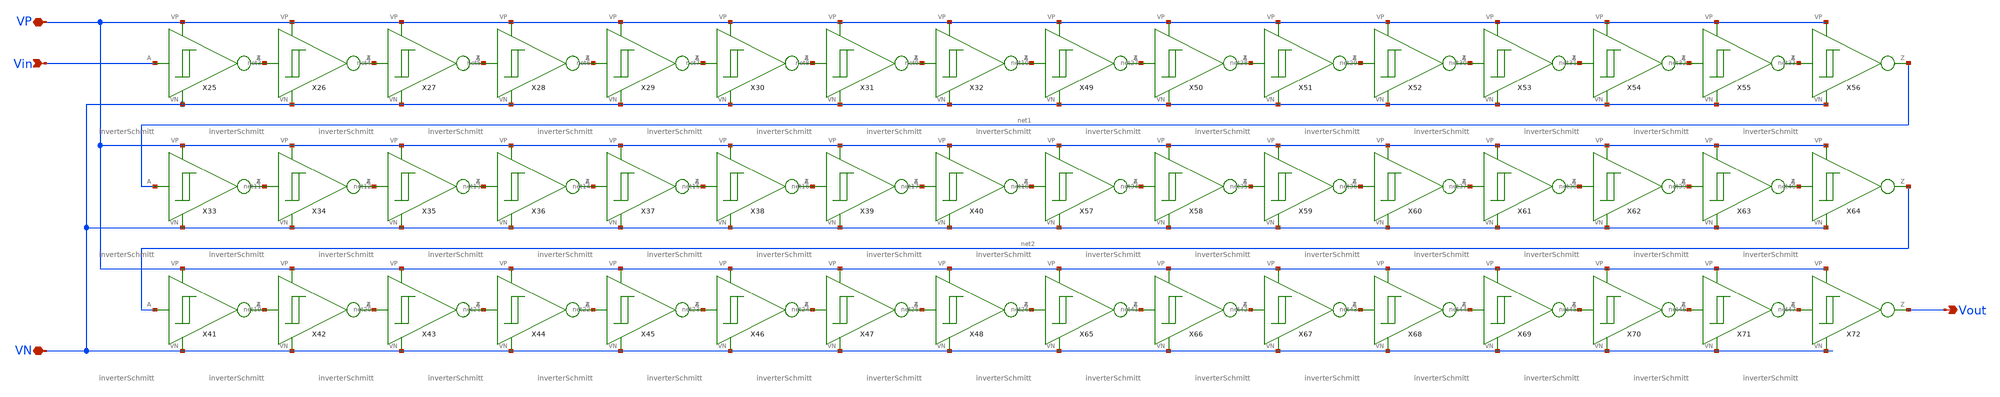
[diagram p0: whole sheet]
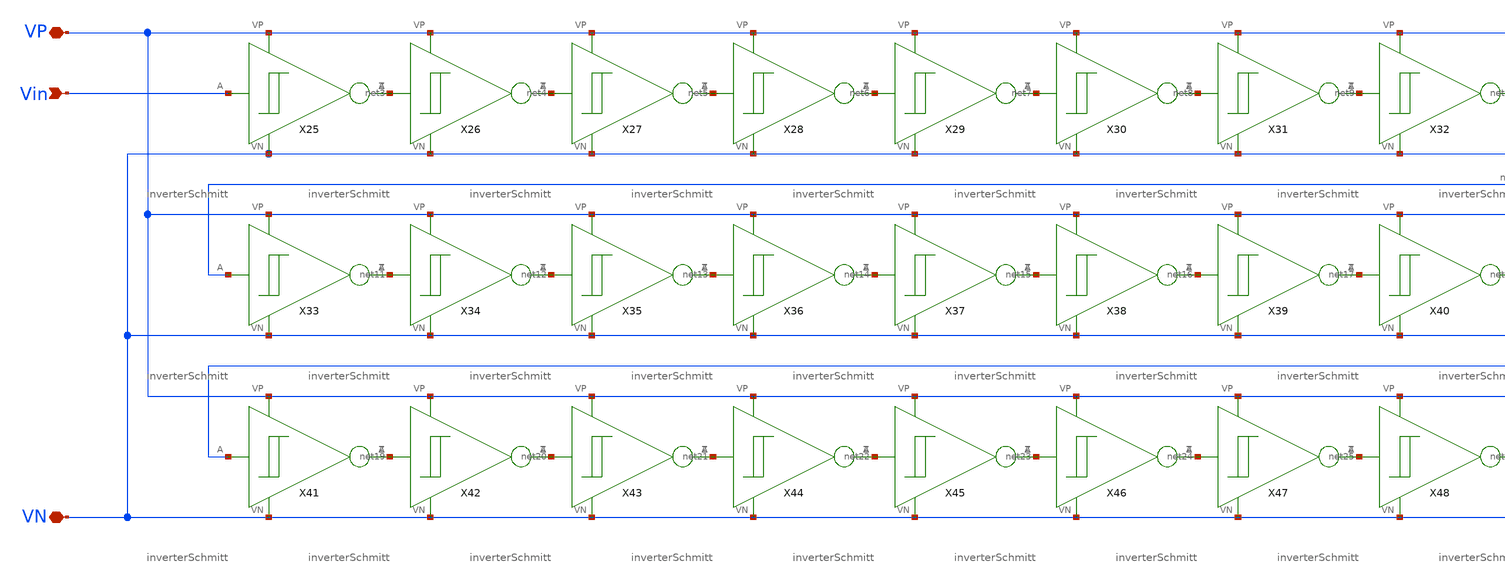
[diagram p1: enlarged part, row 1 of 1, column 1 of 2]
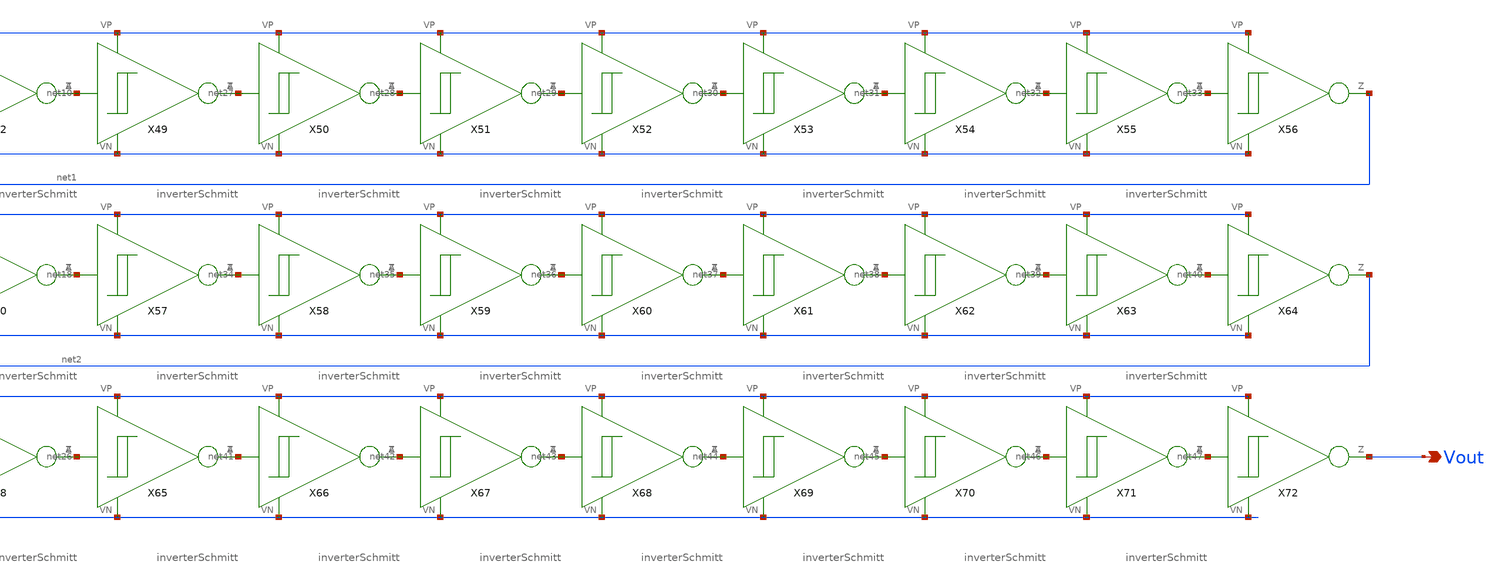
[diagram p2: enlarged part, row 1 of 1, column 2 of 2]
** sch_path: schematics/time_delay.sch
**.subckt time_delay Vin VP VN Vout
*.ipin Vin
*.iopin VP
*.iopin VN
*.opin Vout
X25 Vin VP VN net3 inverterSchmitt
X26 net3 VP VN net4 inverterSchmitt
X27 net4 VP VN net5 inverterSchmitt
X28 net5 VP VN net6 inverterSchmitt
X29 net6 VP VN net7 inverterSchmitt
X30 net7 VP VN net8 inverterSchmitt
X31 net8 VP VN net9 inverterSchmitt
X32 net9 VP VN net10 inverterSchmitt
X33 net1 VP VN net11 inverterSchmitt
X34 net11 VP VN net12 inverterSchmitt
X35 net12 VP VN net13 inverterSchmitt
X36 net13 VP VN net14 inverterSchmitt
X37 net14 VP VN net15 inverterSchmitt
X38 net15 VP VN net16 inverterSchmitt
X39 net16 VP VN net17 inverterSchmitt
X40 net17 VP VN net18 inverterSchmitt
X41 net2 VP VN net19 inverterSchmitt
X42 net19 VP VN net20 inverterSchmitt
X43 net20 VP VN net21 inverterSchmitt
X44 net21 VP VN net22 inverterSchmitt
X45 net22 VP VN net23 inverterSchmitt
X46 net23 VP VN net24 inverterSchmitt
X47 net24 VP VN net25 inverterSchmitt
X48 net25 VP VN net26 inverterSchmitt
X49 net10 VP VN net27 inverterSchmitt
X50 net27 VP VN net28 inverterSchmitt
X51 net28 VP VN net29 inverterSchmitt
X52 net29 VP VN net30 inverterSchmitt
X53 net30 VP VN net31 inverterSchmitt
X54 net31 VP VN net32 inverterSchmitt
X55 net32 VP VN net33 inverterSchmitt
X56 net33 VP VN net1 inverterSchmitt
X57 net18 VP VN net34 inverterSchmitt
X58 net34 VP VN net35 inverterSchmitt
X59 net35 VP VN net36 inverterSchmitt
X60 net36 VP VN net37 inverterSchmitt
X61 net37 VP VN net38 inverterSchmitt
X62 net38 VP VN net39 inverterSchmitt
X63 net39 VP VN net40 inverterSchmitt
X64 net40 VP VN net2 inverterSchmitt
X65 net26 VP VN net41 inverterSchmitt
X66 net41 VP VN net42 inverterSchmitt
X67 net42 VP VN net43 inverterSchmitt
X68 net43 VP VN net44 inverterSchmitt
X69 net44 VP VN net45 inverterSchmitt
X70 net45 VP VN net46 inverterSchmitt
X71 net46 VP VN net47 inverterSchmitt
X72 net47 VP VN Vout inverterSchmitt
**** begin user architecture code

.param l=.15
.param w=1
.param mL=4
.param m=2
.param mS=1

**** end user architecture code
**.ends

* expanding   symbol:  /home/madvlsi/Documents/MADVLSI_final/schematics/inverterSchmitt.sym # of
*+ pins=4
** sym_path: schematics/inverterSchmitt.sym
** sch_path: schematics/inverterSchmitt.sch
.subckt inverterSchmitt A VP VN Z
*.ipin A
*.iopin VP
*.iopin VN
*.opin Z
XM1 net1 A VN GND sky130_fd_pr__nfet_01v8 L=l W=w nf=1 ad='int((nf+1)/2) * W/nf * 0.29' as='int((nf+2)/2) * W/nf * 0.29'
+ pd='2*int((nf+1)/2) * (W/nf + 0.29)' ps='2*int((nf+2)/2) * (W/nf + 0.29)' nrd='0.29 / W' nrs='0.29 / W'
+ sa=0 sb=0 sd=0 mult=m m=m
XM2 net1 A VP VDD sky130_fd_pr__pfet_01v8 L=l W=w nf=1 ad='int((nf+1)/2) * W/nf * 0.29' as='int((nf+2)/2) * W/nf * 0.29'
+ pd='2*int((nf+1)/2) * (W/nf + 0.29)' ps='2*int((nf+2)/2) * (W/nf + 0.29)' nrd='0.29 / W' nrs='0.29 / W'
+ sa=0 sb=0 sd=0 mult=mL m=mL
XM5 net2 net1 VP VDD sky130_fd_pr__pfet_01v8 L=l W=w nf=1 ad='int((nf+1)/2) * W/nf * 0.29' as='int((nf+2)/2) * W/nf * 0.29'
+ pd='2*int((nf+1)/2) * (W/nf + 0.29)' ps='2*int((nf+2)/2) * (W/nf + 0.29)' nrd='0.29 / W' nrs='0.29 / W'
+ sa=0 sb=0 sd=0 mult=mL m=mL
XM6 net2 net1 VN GND sky130_fd_pr__nfet_01v8 L=l W=w nf=1 ad='int((nf+1)/2) * W/nf * 0.29' as='int((nf+2)/2) * W/nf * 0.29'
+ pd='2*int((nf+1)/2) * (W/nf + 0.29)' ps='2*int((nf+2)/2) * (W/nf + 0.29)' nrd='0.29 / W' nrs='0.29 / W'
+ sa=0 sb=0 sd=0 mult=m m=m
XM3 VP net2 net1 VP sky130_fd_pr__pfet_01v8 L=l W=w nf=1 ad='int((nf+1)/2) * W/nf * 0.29' as='int((nf+2)/2) * W/nf * 0.29'
+ pd='2*int((nf+1)/2) * (W/nf + 0.29)' ps='2*int((nf+2)/2) * (W/nf + 0.29)' nrd='0.29 / W' nrs='0.29 / W'
+ sa=0 sb=0 sd=0 mult=m m=m
XM4 VN net2 net1 VN sky130_fd_pr__nfet_01v8 L=l W=w nf=1 ad='int((nf+1)/2) * W/nf * 0.29' as='int((nf+2)/2) * W/nf * 0.29'
+ pd='2*int((nf+1)/2) * (W/nf + 0.29)' ps='2*int((nf+2)/2) * (W/nf + 0.29)' nrd='0.29 / W' nrs='0.29 / W'
+ sa=0 sb=0 sd=0 mult=mS m=mS
XM7 Z net2 VP VDD sky130_fd_pr__pfet_01v8 L=l W=w nf=1 ad='int((nf+1)/2) * W/nf * 0.29' as='int((nf+2)/2) * W/nf * 0.29'
+ pd='2*int((nf+1)/2) * (W/nf + 0.29)' ps='2*int((nf+2)/2) * (W/nf + 0.29)' nrd='0.29 / W' nrs='0.29 / W'
+ sa=0 sb=0 sd=0 mult=mL m=mL
XM8 Z net2 VN GND sky130_fd_pr__nfet_01v8 L=l W=w nf=1 ad='int((nf+1)/2) * W/nf * 0.29' as='int((nf+2)/2) * W/nf * 0.29'
+ pd='2*int((nf+1)/2) * (W/nf + 0.29)' ps='2*int((nf+2)/2) * (W/nf + 0.29)' nrd='0.29 / W' nrs='0.29 / W'
+ sa=0 sb=0 sd=0 mult=m m=m
**** begin user architecture code

.param l=.15
.param w=1
.param mL=4
.param mS=1
.param m=2

**** end user architecture code
.ends

.end
